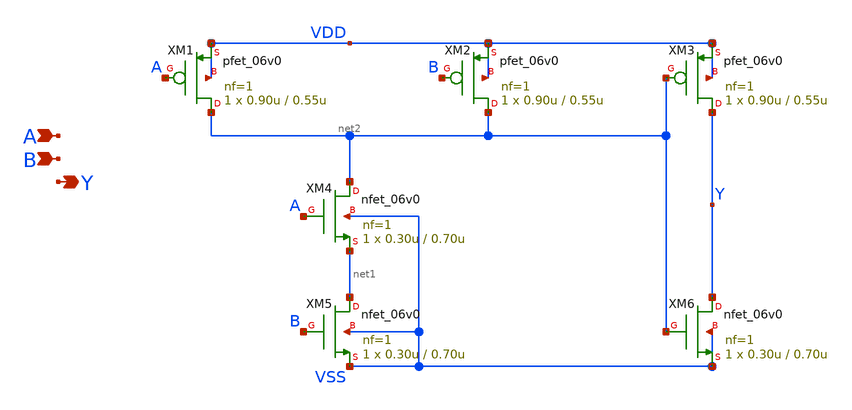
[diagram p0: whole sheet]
** sch_path: designs/libs/core_analog/digital/digital_and2_1.sch
**.subckt digital_and2_1 A B Y
*.ipin A
*.ipin B
*.opin Y
XM1 net2 A VDD VDD pfet_06v0 L=0.55u W=0.90u nf=1 ad='int((nf+1)/2) * W/nf * 0.18u' as='int((nf+2)/2) * W/nf * 0.18u'
+ pd='2*int((nf+1)/2) * (W/nf + 0.18u)' ps='2*int((nf+2)/2) * (W/nf + 0.18u)' nrd='0.18u / W' nrs='0.18u / W'
+ sa=0 sb=0 sd=0 m=1
XM2 net2 B VDD VDD pfet_06v0 L=0.55u W=0.90u nf=1 ad='int((nf+1)/2) * W/nf * 0.18u' as='int((nf+2)/2) * W/nf * 0.18u'
+ pd='2*int((nf+1)/2) * (W/nf + 0.18u)' ps='2*int((nf+2)/2) * (W/nf + 0.18u)' nrd='0.18u / W' nrs='0.18u / W'
+ sa=0 sb=0 sd=0 m=1
XM3 Y net2 VDD VDD pfet_06v0 L=0.55u W=0.90u nf=1 ad='int((nf+1)/2) * W/nf * 0.18u' as='int((nf+2)/2) * W/nf * 0.18u'
+ pd='2*int((nf+1)/2) * (W/nf + 0.18u)' ps='2*int((nf+2)/2) * (W/nf + 0.18u)' nrd='0.18u / W' nrs='0.18u / W'
+ sa=0 sb=0 sd=0 m=1
XM4 net2 A net1 VSS nfet_06v0 L=0.70u W=0.30u nf=1 ad='int((nf+1)/2) * W/nf * 0.18u' as='int((nf+2)/2) * W/nf * 0.18u'
+ pd='2*int((nf+1)/2) * (W/nf + 0.18u)' ps='2*int((nf+2)/2) * (W/nf + 0.18u)' nrd='0.18u / W' nrs='0.18u / W'
+ sa=0 sb=0 sd=0 m=1
XM5 net1 B VSS VSS nfet_06v0 L=0.70u W=0.30u nf=1 ad='int((nf+1)/2) * W/nf * 0.18u' as='int((nf+2)/2) * W/nf * 0.18u'
+ pd='2*int((nf+1)/2) * (W/nf + 0.18u)' ps='2*int((nf+2)/2) * (W/nf + 0.18u)' nrd='0.18u / W' nrs='0.18u / W'
+ sa=0 sb=0 sd=0 m=1
XM6 Y net2 VSS VSS nfet_06v0 L=0.70u W=0.30u nf=1 ad='int((nf+1)/2) * W/nf * 0.18u' as='int((nf+2)/2) * W/nf * 0.18u'
+ pd='2*int((nf+1)/2) * (W/nf + 0.18u)' ps='2*int((nf+2)/2) * (W/nf + 0.18u)' nrd='0.18u / W' nrs='0.18u / W'
+ sa=0 sb=0 sd=0 m=1
**.ends
.end
